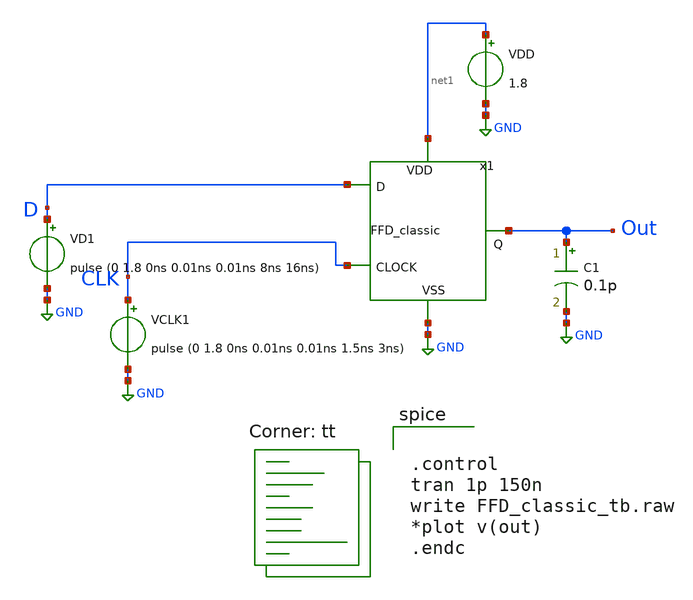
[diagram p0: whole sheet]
** sch_path: FFD_classic_tb.sch
**.subckt FFD_classic_tb
VDD net1 GND 1.8
C1 Out GND 0.1p m=1
x1 Out D net1 CLK GND FFD_classic
VD1 D GND pulse (0 1.8 0ns 0.01ns 0.01ns 8ns 16ns)
VCLK1 CLK GND pulse (0 1.8 0ns 0.01ns 0.01ns 1.5ns 3ns)
**** begin user architecture code
.lib $::SKYWATER_MODELS/sky130.lib.spice tt


.control
tran 1p 150n
write FFD_classic_tb.raw
*plot v(out)
.endc


**** end user architecture code
**.ends
.GLOBAL GND
.end
